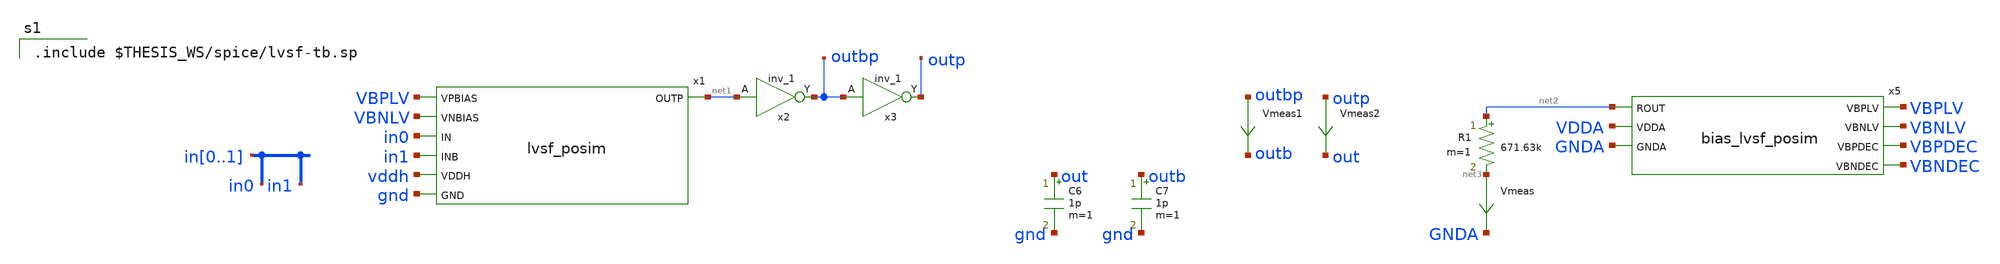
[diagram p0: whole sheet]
** sch_path: xschem/lvsf-tb.sch
.lib $::SKYWATER_MODELS/sky130.lib.spice sf
.include ~/pdk/sky130A/libs.ref/sky130_fd_sc_hvl/spice/sky130_fd_sc_hvl.spice

**.subckt lvsf-tb
C6 out gnd 1p m=1
C7 outb gnd 1p m=1
Vmeas1 outbp outb 0
.save i(vmeas1)
Vmeas2 outp out 0
.save i(vmeas2)
x1 VBPLV VBNLV in0 in1 net1 vddh gnd lvsf_posim
x2 net1 GND GND VDDH VDDH outbp sky130_fd_sc_hvl__inv_1
x3 outbp GND GND VDDH VDDH outp sky130_fd_sc_hvl__inv_1
R1 net2 net3 671.63k m=1
Vmeas net3 GNDA 0
.save i(vmeas)
x5 net2 VBPLV VBNLV VBPDEC VBNDEC VDDA GNDA bias_lvsf_posim
**** begin user architecture code

.include $THESIS_WS/spice/lvsf-tb.sp

**** end user architecture code
**.ends
.end
